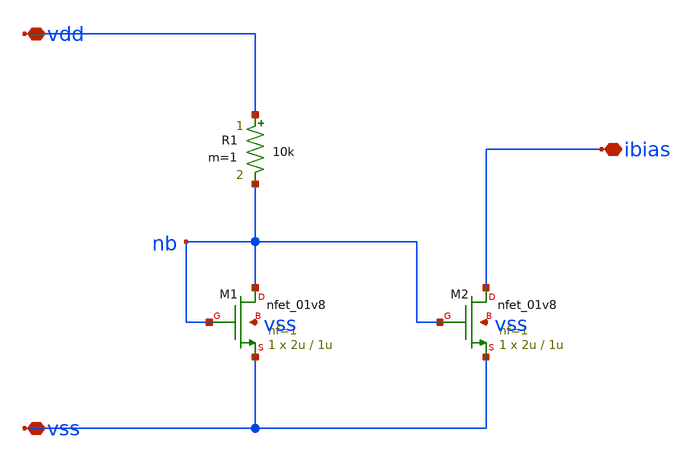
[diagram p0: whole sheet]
** sch_path: examples/demo_tapeout/xschem/kv_bias.sch
**.subckt kv_bias vdd vss ibias
*.iopin vdd
*.iopin vss
*.iopin ibias
R1 vdd nb 10k m=1
XM1 nb nb vss vss sky130_fd_pr__nfet_01v8 L=1u W=2u nf=1 ad='int((1 + 1)/2) * 2u / 1 * 0.29' as='int((1 + 2)/2) * 2u / 1 * 0.29'
+ pd='2*int((1 + 1)/2) * (2u / 1 + 0.29)' ps='2*int((1 + 2)/2) * (2u / 1 + 0.29)' nrd='0.29 / 2u ' nrs='0.29 / 2u '
+ sa=0 sb=0 sd=0 mult=1 m=1
XM2 ibias nb vss vss sky130_fd_pr__nfet_01v8 L=1u W=2u nf=1 ad='int((1 + 1)/2) * 2u / 1 * 0.29' as='int((1 + 2)/2) * 2u / 1 * 0.29'
+ pd='2*int((1 + 1)/2) * (2u / 1 + 0.29)' ps='2*int((1 + 2)/2) * (2u / 1 + 0.29)' nrd='0.29 / 2u ' nrs='0.29 / 2u '
+ sa=0 sb=0 sd=0 mult=1 m=1
**.ends
.end
